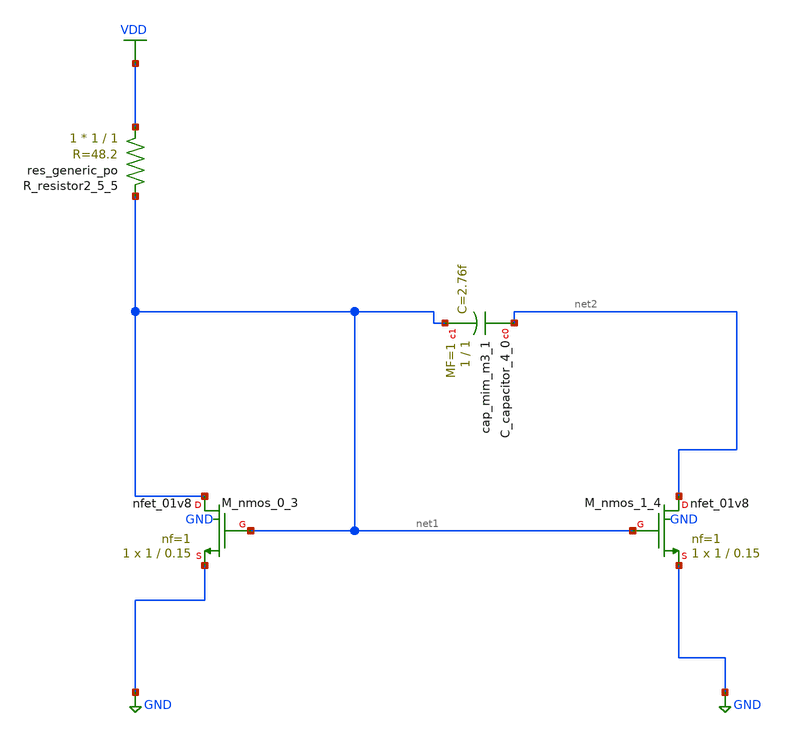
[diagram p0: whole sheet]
** sch_path: schematics/AMSNet/340.sch
**.subckt 340
XC_capacitor_4_0 net2 net1 sky130_fd_pr__cap_mim_m3_1 W=1 L=1 MF=1 m=1
XM_nmos_0_3 net1 net1 GND GND sky130_fd_pr__nfet_01v8 L=0.15 W=1 nf=1 ad='int((1 + 1)/2) * 1 / 1 * 0.29'
+ as='int((1 + 2)/2) * 1 / 1 * 0.29' pd='2*int((1 + 1)/2) * (1 / 1 + 0.29)' ps='2*int((1 + 2)/2) * (1 / 1 + 0.29)'
+ nrd='0.29 / 1 ' nrs='0.29 / 1 ' sa=0 sb=0 sd=0 mult=1 m=1
XM_nmos_1_4 net2 net1 GND GND sky130_fd_pr__nfet_01v8 L=0.15 W=1 nf=1 ad='int((1 + 1)/2) * 1 / 1 * 0.29'
+ as='int((1 + 2)/2) * 1 / 1 * 0.29' pd='2*int((1 + 1)/2) * (1 / 1 + 0.29)' ps='2*int((1 + 2)/2) * (1 / 1 + 0.29)'
+ nrd='0.29 / 1 ' nrs='0.29 / 1 ' sa=0 sb=0 sd=0 mult=1 m=1
XR_resistor2_5_5 VDD net1 sky130_fd_pr__res_generic_po W=1 L=1 m=1
**.ends
.GLOBAL GND
.GLOBAL VDD
.end
